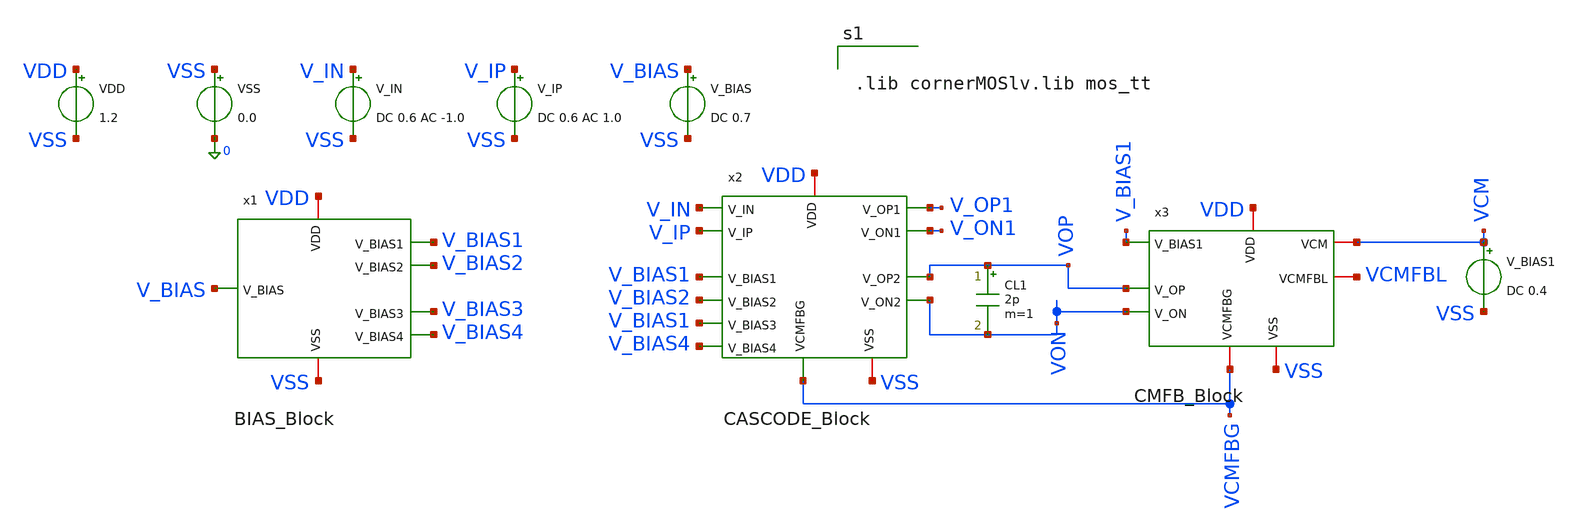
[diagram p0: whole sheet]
** sch_path: two-stage-ota-with-cmfb/Simulation/TEST_NOISE.sch
**.subckt TEST_NOISE
VDD VDD VSS 1.2
VSS VSS 0 0.0
V_IN V_IN VSS DC 0.6 AC -1.0
V_IP V_IP VSS DC 0.6 AC 1.0
V_BIAS V_BIAS VSS DC 0.7
V_BIAS1 VCM VSS DC 0.4
CL1 VOP VON 2p m=1
x1 VSS V_BIAS4 V_BIAS2 V_BIAS3 VDD V_BIAS1 V_BIAS BIAS_Block
x2 VDD V_BIAS1 V_IN V_IP V_BIAS2 V_ON1 V_OP1 V_BIAS1 VON VOP VCMFBG V_BIAS4 VSS CASCODE_Block
x3 VDD V_BIAS1 VCM VOP VON VCMFBL VCMFBG VSS CMFB_Block
**** begin user architecture code


.lib cornerMOSlv.lib mos_tt




* ==============================================================================
* MUC D: NOISE SIMULATION (FULL OUTPUT & 1/f CORNER EXTRACTION)
* ==============================================================================

.control
set color0=white
set color1=black

echo '=========================================================================='
echo '  D. NOISE ANALYSIS: INPUT-REFERRED NOISE, 1/f CORNER & INTEGRATED NOISE'
echo '=========================================================================='

* 1. Chay phan tich Noise tu 1 Hz den GBW = 200 MHz, 20 diem moi decade
noise v(vop,von) v_ip dec 20 1 200Meg

* 2. Lay ket qua tu plot chua pho nhieu (noise1)
setplot noise1

* Doi don vi sang nV/sqrt(Hz) de ve va hien thi
let irn_nv = inoise_spectrum * 1e9
let orn_nv = onoise_spectrum * 1e9

* --- TRICH XUAT SAN NHIEU TRANG (WHITE NOISE FLOOR) ---
* Lay gia tri mat do nhieu o vung tan so cao
let len = length(inoise_spectrum)
let white_floor = inoise_spectrum[len - 10]
let white_floor_nv = white_floor * 1e9

* --- TRICH XUAT 1/f CORNER FREQUENCY (fc) ---
* Tai fc, mat do nhieu = sqrt(2) * white_floor = 1.4142 * white_floor
let target_val = white_floor * 1.41421356

let idx = 0
while (inoise_spectrum[idx] > target_val and idx < len - 1)
  let idx = idx + 1
end

let f_corner = frequency[idx]

* 3. Lay tong nhieu tich luy tu plot noise2
setplot noise2
let rms_in  = inoise_total
let rms_out = onoise_total

echo '--------------------------------------------------------------------------'
echo 'KET QUA NOISE SIMULATION (1 Hz den GBW = 200 MHz):'
echo '--------------------------------------------------------------------------'
setplot noise1
print white_floor_nv
print f_corner
setplot noise2
print rms_in rms_out
echo '--------------------------------------------------------------------------'

* Quay lai plot noise1 de ve 2 do thi pho mat do nhieu
setplot noise1

* Ve pho mat do nhieu quy doi ve ngo vao (Input-Referred Noise)
plot irn_nv xlog ylabel 'Input Noise Density (nV/sqrt(Hz))' xlabel 'Frequency (Hz)' title 'Input-Referred Noise Spectral Density'

* Ve pho mat do nhieu tai ngo ra (Output Noise)
plot orn_nv xlog ylabel 'Output Noise Density (nV/sqrt(Hz))' xlabel 'Frequency (Hz)' title 'Output Noise Spectral Density'

* 4. In bang chi tiet dong gop nhieu cua tat ca transistor
setplot noise2
echo '--------------------------------------------------------------------------'
echo 'DONG GOP NHIEU CUA TUNG LINH KIEN (PRINT NOISE SUMMARY):'
echo '--------------------------------------------------------------------------'
print all
echo '--------------------------------------------------------------------------'

.endc


**** end user architecture code
**.ends
.end
